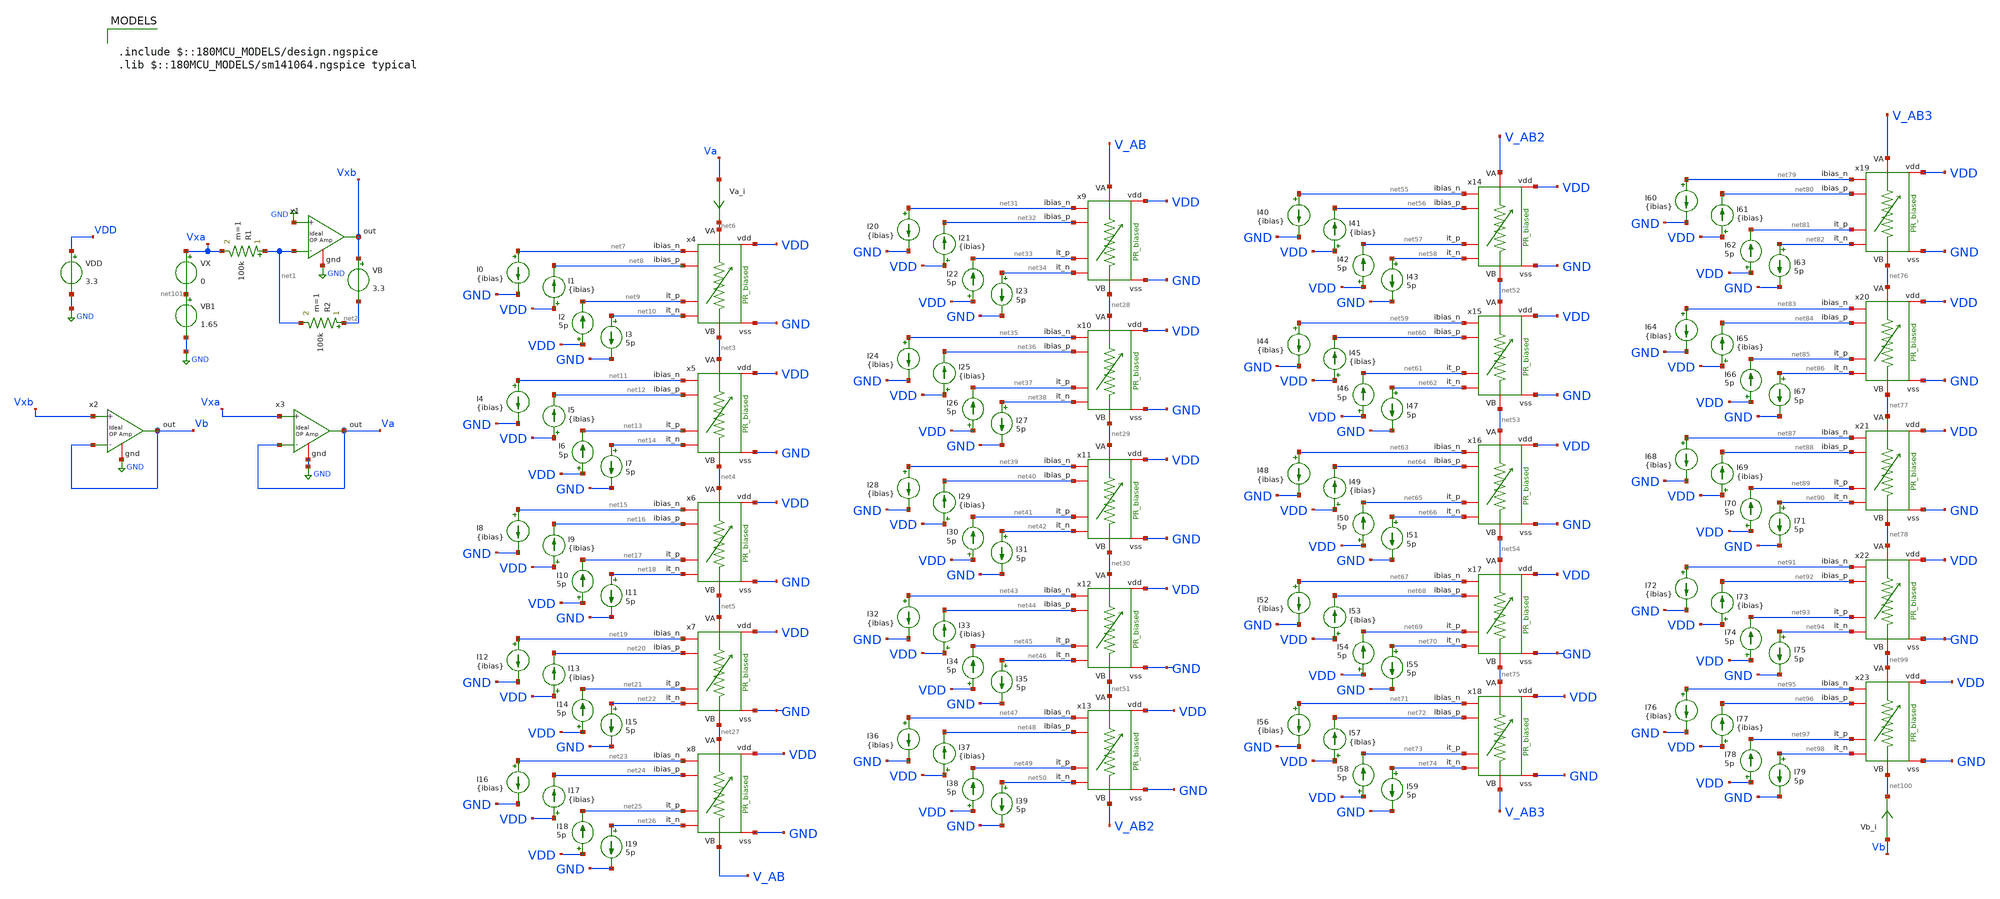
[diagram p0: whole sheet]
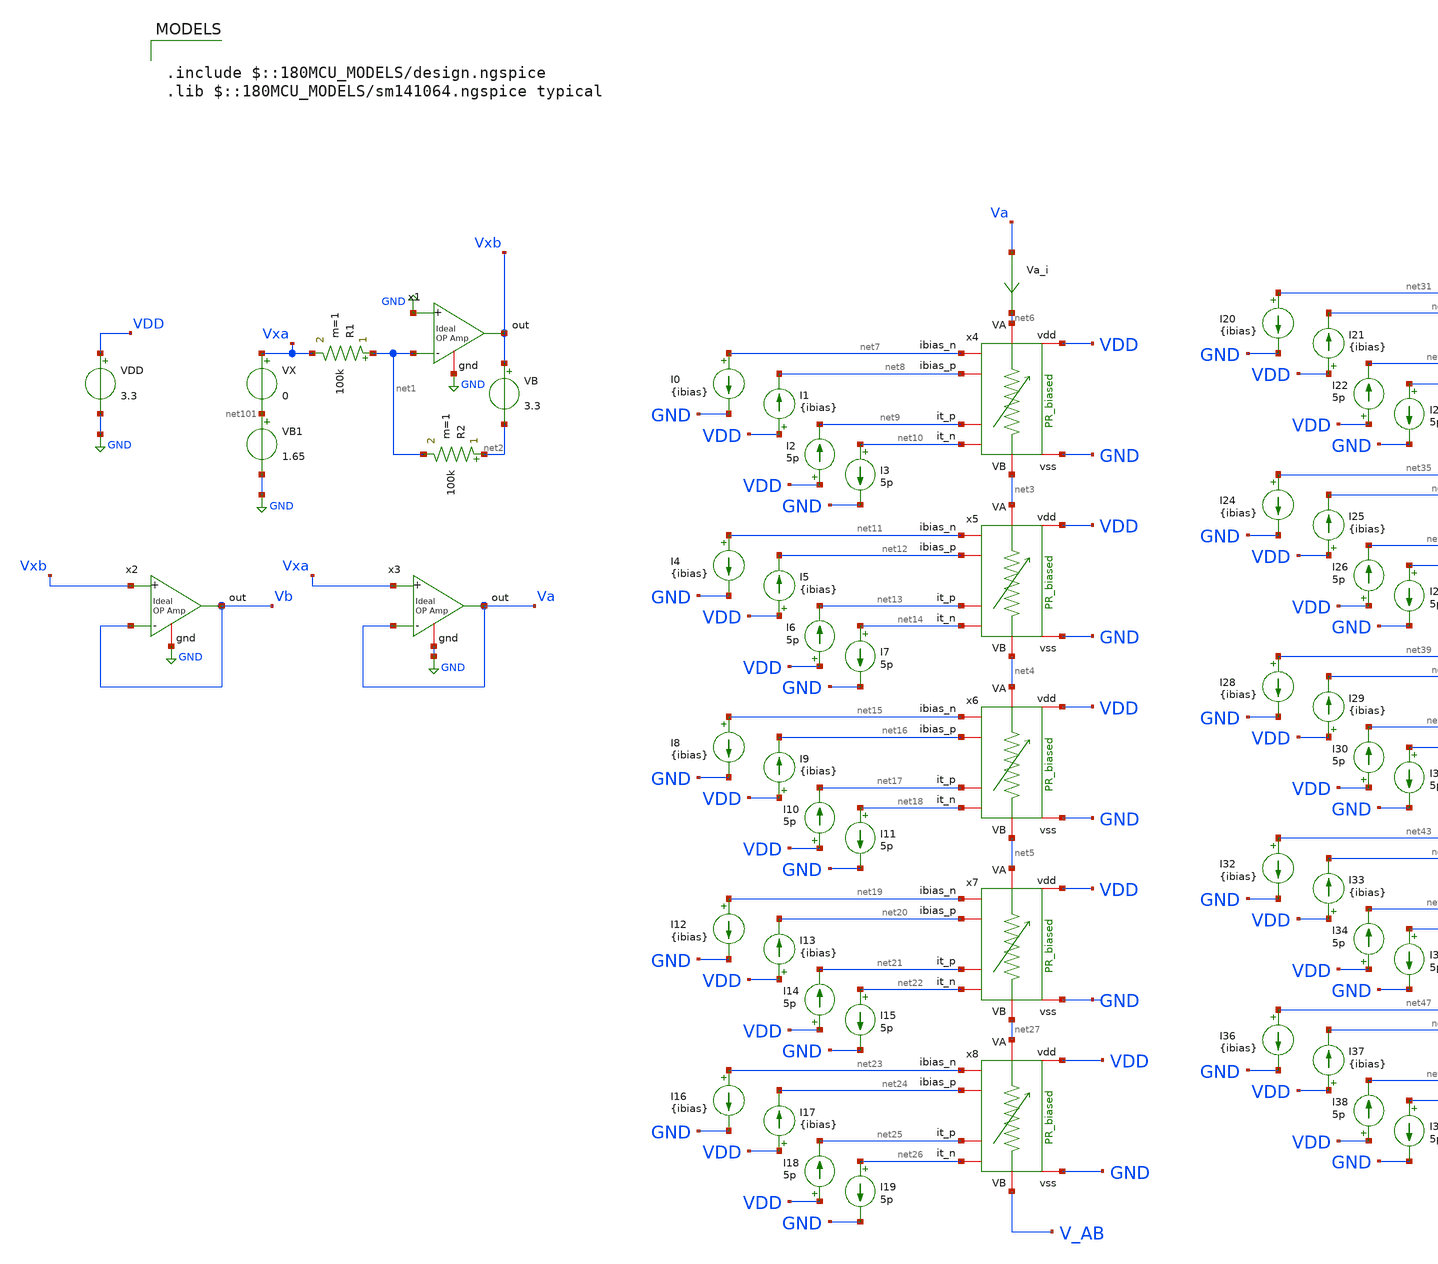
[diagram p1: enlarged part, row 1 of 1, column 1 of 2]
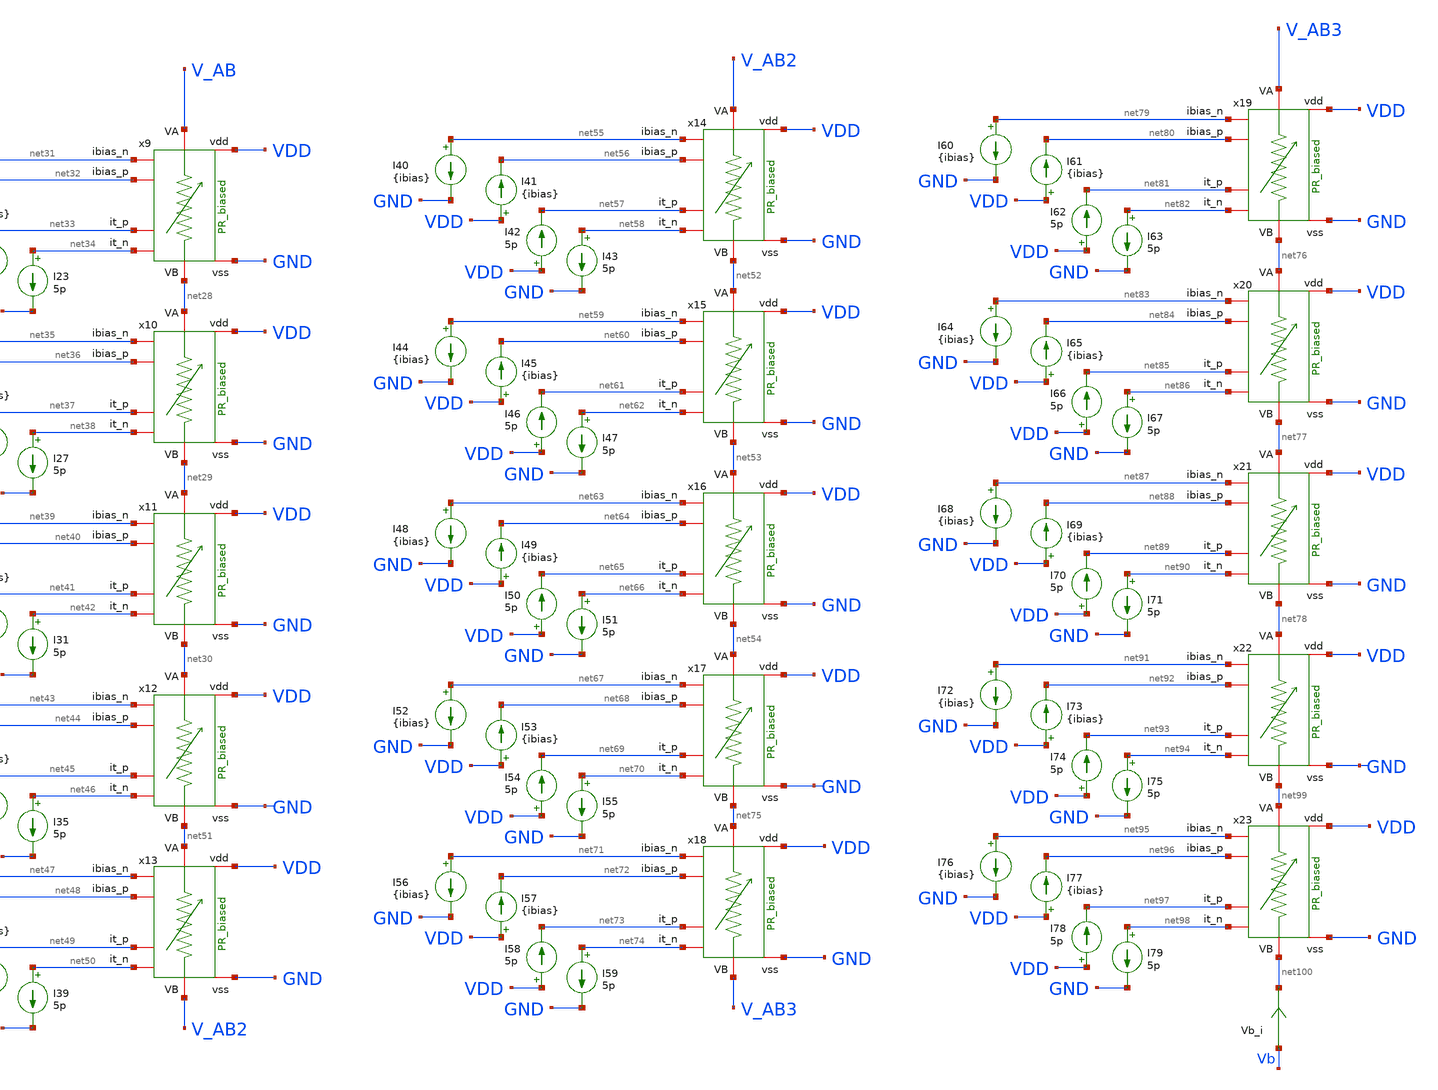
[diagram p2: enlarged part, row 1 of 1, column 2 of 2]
** sch_path: TIA/xschem/pseudo_res_dir/TB_PR_Series.sch
**.subckt TB_PR_Series
VDD VDD GND 3.3
VX Vxa net101 0
VB Vxb net2 3.3
R1 net1 Vxa 100k m=1
R2 net2 net1 100k m=1
VB1 net101 GND 1.65
x1 Vxb GND net1 GND ampOp_ideal
x2 Vb Vxb Vb GND ampOp_ideal
x3 Va Vxa Va GND ampOp_ideal
x4 VDD GND net6 net3 net8 net10 net9 net7 PR_biased
x5 VDD GND net3 net4 net12 net14 net13 net11 PR_biased
x6 VDD GND net4 net5 net16 net18 net17 net15 PR_biased
x7 VDD GND net5 net27 net20 net22 net21 net19 PR_biased
x8 VDD GND net27 V_AB net24 net26 net25 net23 PR_biased
Va_i Va net6 0
.save i(va_i)
Vb_i Vb net100 0
.save i(vb_i)
I0 net7 GND {ibias}
I1 VDD net8 {ibias}
I2 VDD net9 5p
I3 net10 GND 5p
I4 net11 GND {ibias}
I5 VDD net12 {ibias}
I6 VDD net13 5p
I7 net14 GND 5p
I8 net15 GND {ibias}
I9 VDD net16 {ibias}
I10 VDD net17 5p
I11 net18 GND 5p
I12 net19 GND {ibias}
I13 VDD net20 {ibias}
I14 VDD net21 5p
I15 net22 GND 5p
I16 net23 GND {ibias}
I17 VDD net24 {ibias}
I18 VDD net25 5p
I19 net26 GND 5p
x9 VDD GND V_AB net28 net32 net34 net33 net31 PR_biased
x10 VDD GND net28 net29 net36 net38 net37 net35 PR_biased
x11 VDD GND net29 net30 net40 net42 net41 net39 PR_biased
x12 VDD GND net30 net51 net44 net46 net45 net43 PR_biased
x13 VDD GND net51 V_AB2 net48 net50 net49 net47 PR_biased
I20 net31 GND {ibias}
I21 VDD net32 {ibias}
I22 VDD net33 5p
I23 net34 GND 5p
I24 net35 GND {ibias}
I25 VDD net36 {ibias}
I26 VDD net37 5p
I27 net38 GND 5p
I28 net39 GND {ibias}
I29 VDD net40 {ibias}
I30 VDD net41 5p
I31 net42 GND 5p
I32 net43 GND {ibias}
I33 VDD net44 {ibias}
I34 VDD net45 5p
I35 net46 GND 5p
I36 net47 GND {ibias}
I37 VDD net48 {ibias}
I38 VDD net49 5p
I39 net50 GND 5p
x14 VDD GND V_AB2 net52 net56 net58 net57 net55 PR_biased
x15 VDD GND net52 net53 net60 net62 net61 net59 PR_biased
x16 VDD GND net53 net54 net64 net66 net65 net63 PR_biased
x17 VDD GND net54 net75 net68 net70 net69 net67 PR_biased
x18 VDD GND net75 V_AB3 net72 net74 net73 net71 PR_biased
I40 net55 GND {ibias}
I41 VDD net56 {ibias}
I42 VDD net57 5p
I43 net58 GND 5p
I44 net59 GND {ibias}
I45 VDD net60 {ibias}
I46 VDD net61 5p
I47 net62 GND 5p
I48 net63 GND {ibias}
I49 VDD net64 {ibias}
I50 VDD net65 5p
I51 net66 GND 5p
I52 net67 GND {ibias}
I53 VDD net68 {ibias}
I54 VDD net69 5p
I55 net70 GND 5p
I56 net71 GND {ibias}
I57 VDD net72 {ibias}
I58 VDD net73 5p
I59 net74 GND 5p
x19 VDD GND V_AB3 net76 net80 net82 net81 net79 PR_biased
x20 VDD GND net76 net77 net84 net86 net85 net83 PR_biased
x21 VDD GND net77 net78 net88 net90 net89 net87 PR_biased
x22 VDD GND net78 net99 net92 net94 net93 net91 PR_biased
x23 VDD GND net99 net100 net96 net98 net97 net95 PR_biased
I60 net79 GND {ibias}
I61 VDD net80 {ibias}
I62 VDD net81 5p
I63 net82 GND 5p
I64 net83 GND {ibias}
I65 VDD net84 {ibias}
I66 VDD net85 5p
I67 net86 GND 5p
I68 net87 GND {ibias}
I69 VDD net88 {ibias}
I70 VDD net89 5p
I71 net90 GND 5p
I72 net91 GND {ibias}
I73 VDD net92 {ibias}
I74 VDD net93 5p
I75 net94 GND 5p
I76 net95 GND {ibias}
I77 VDD net96 {ibias}
I78 VDD net97 5p
I79 net98 GND 5p
**** begin user architecture code

.include $::180MCU_MODELS/design.ngspice
.lib $::180MCU_MODELS/sm141064.ngspice typical



*.option savecurrents
.option gmin=1e-24

.param ibias = 5p
*.param it_amp = 5p

.control
save all

op
remzerovec
set filetype = binary
write TB_PR_Series.raw
set appendwrite

dc VX -500m 500m 10m

let idiff = i(Va_i)-i(Vb_i)
let Rdiff = 4/deriv(idiff)

save idiff Rdiff
remzerovec

write TB_PR_Series.raw

.endc


**** end user architecture code
**.ends
.GLOBAL GND
.end
